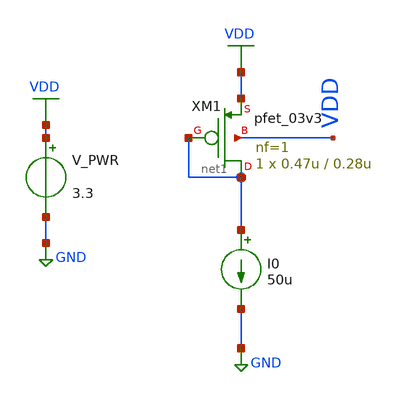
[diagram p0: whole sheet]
** sch_path: src/design_tb/p_res.sch
**.subckt p_res
XM1 net1 net1 VDD VDD pfet_03v3 L=0.28u W=0.47u nf=1 ad='int((nf+1)/2) * W/nf * 0.18u' as='int((nf+2)/2) * W/nf * 0.18u'
+ pd='2*int((nf+1)/2) * (W/nf + 0.18u)' ps='2*int((nf+2)/2) * (W/nf + 0.18u)' nrd='0.18u / W' nrs='0.18u / W'
+ sa=0 sb=0 sd=0 m=1
I0 net1 GND 50u
V_PWR VDD GND 3.3
.save i(v_pwr)
**** begin user architecture code

.include $::180MCU_MODELS/design.ngspice
.lib $::180MCU_MODELS/sm141064.ngspice typical
.lib $::180MCU_MODELS/sm141064.ngspice mimcap_typical
.lib $::180MCU_MODELS/sm141064.ngspice cap_mim
.lib $::180MCU_MODELS/sm141064.ngspice res_typical




*.op
*.save all

.control
save all
op
print @m.xm1.m0[gm]
set appendwrite
write pres_tb.raw
.endc


**** end user architecture code
**.ends
.GLOBAL GND
.GLOBAL VDD
.end
